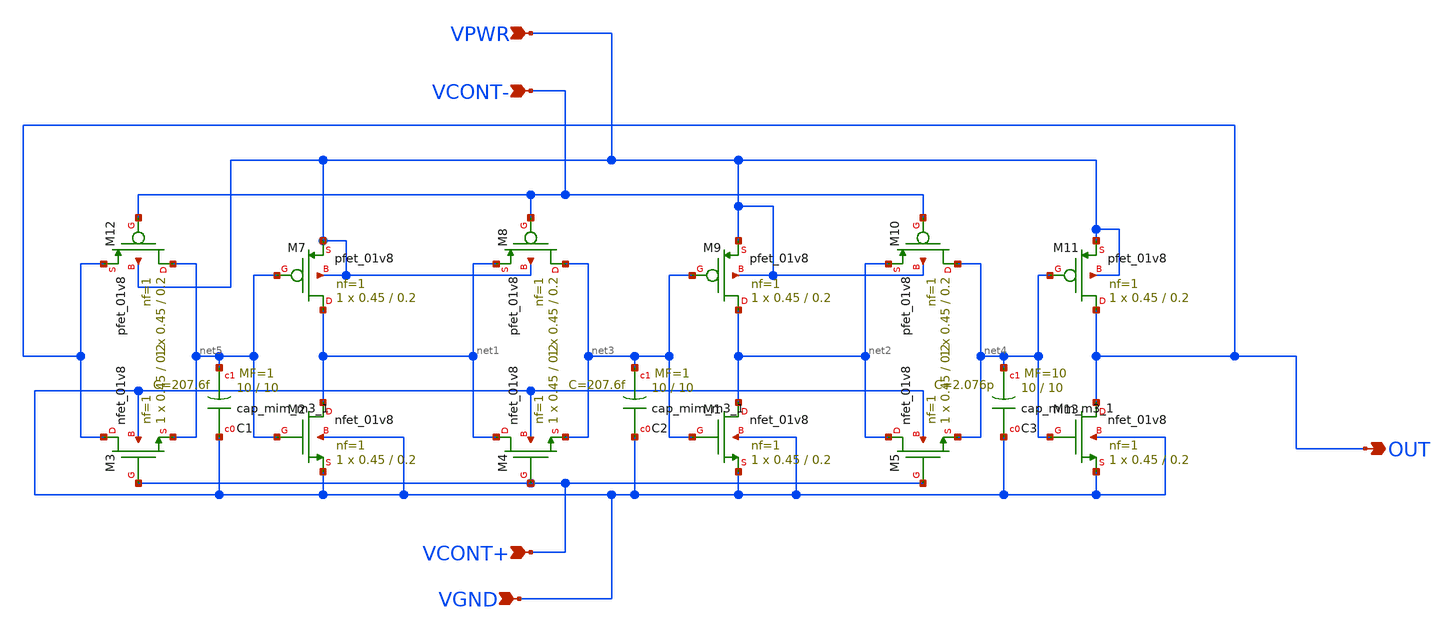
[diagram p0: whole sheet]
** sch_path: xschem_sch/ring-oscillator_with_tg.sch
**.subckt ring-oscillator_with_tg VPWR OUT VGND VCONT+ VCONT-
*.ipin VPWR
*.opin OUT
*.ipin VGND
*.ipin VCONT+
*.ipin VCONT-
XM7 net1 net5 VPWR VPWR sky130_fd_pr__pfet_01v8 L=0.2 W=0.45 nf=1 ad='int((nf+1)/2) * W/nf * 0.29' as='int((nf+2)/2) * W/nf * 0.29'
+ pd='2*int((nf+1)/2) * (W/nf + 0.29)' ps='2*int((nf+2)/2) * (W/nf + 0.29)' nrd='0.29 / W' nrs='0.29 / W'
+ sa=0 sb=0 sd=0 mult=1 m=1
XM8 net3 VCONT- net1 VPWR sky130_fd_pr__pfet_01v8 L=0.2 W=0.45 nf=1 ad='int((nf+1)/2) * W/nf * 0.29'
+ as='int((nf+2)/2) * W/nf * 0.29' pd='2*int((nf+1)/2) * (W/nf + 0.29)' ps='2*int((nf+2)/2) * (W/nf + 0.29)'
+ nrd='0.29 / W' nrs='0.29 / W' sa=0 sb=0 sd=0 mult=1 m=1
XM9 net2 net3 VPWR VPWR sky130_fd_pr__pfet_01v8 L=0.2 W=0.45 nf=1 ad='int((nf+1)/2) * W/nf * 0.29' as='int((nf+2)/2) * W/nf * 0.29'
+ pd='2*int((nf+1)/2) * (W/nf + 0.29)' ps='2*int((nf+2)/2) * (W/nf + 0.29)' nrd='0.29 / W' nrs='0.29 / W'
+ sa=0 sb=0 sd=0 mult=1 m=1
XM11 OUT net4 VPWR VPWR sky130_fd_pr__pfet_01v8 L=0.2 W=0.45 nf=1 ad='int((nf+1)/2) * W/nf * 0.29' as='int((nf+2)/2) * W/nf * 0.29'
+ pd='2*int((nf+1)/2) * (W/nf + 0.29)' ps='2*int((nf+2)/2) * (W/nf + 0.29)' nrd='0.29 / W' nrs='0.29 / W'
+ sa=0 sb=0 sd=0 mult=1 m=1
XM10 net4 VCONT- net2 VPWR sky130_fd_pr__pfet_01v8 L=0.2 W=0.45 nf=1 ad='int((nf+1)/2) * W/nf * 0.29'
+ as='int((nf+2)/2) * W/nf * 0.29' pd='2*int((nf+1)/2) * (W/nf + 0.29)' ps='2*int((nf+2)/2) * (W/nf + 0.29)'
+ nrd='0.29 / W' nrs='0.29 / W' sa=0 sb=0 sd=0 mult=1 m=1
XM12 net5 VCONT- OUT VPWR sky130_fd_pr__pfet_01v8 L=0.2 W=0.45 nf=1 ad='int((nf+1)/2) * W/nf * 0.29'
+ as='int((nf+2)/2) * W/nf * 0.29' pd='2*int((nf+1)/2) * (W/nf + 0.29)' ps='2*int((nf+2)/2) * (W/nf + 0.29)'
+ nrd='0.29 / W' nrs='0.29 / W' sa=0 sb=0 sd=0 mult=1 m=1
XC1 VGND net5 sky130_fd_pr__cap_mim_m3_1 W=10 L=10 MF=1 m=1
XC2 VGND net3 sky130_fd_pr__cap_mim_m3_1 W=10 L=10 MF=1 m=1
XC3 VGND net4 sky130_fd_pr__cap_mim_m3_1 W=10 L=10 MF=10 m=10
XM13 OUT net4 VGND VGND sky130_fd_pr__nfet_01v8 L=0.2 W=0.45 nf=1 ad='int((nf+1)/2) * W/nf * 0.29' as='int((nf+2)/2) * W/nf * 0.29'
+ pd='2*int((nf+1)/2) * (W/nf + 0.29)' ps='2*int((nf+2)/2) * (W/nf + 0.29)' nrd='0.29 / W' nrs='0.29 / W'
+ sa=0 sb=0 sd=0 mult=1 m=1
XM1 net2 net3 VGND VGND sky130_fd_pr__nfet_01v8 L=0.2 W=0.45 nf=1 ad='int((nf+1)/2) * W/nf * 0.29' as='int((nf+2)/2) * W/nf * 0.29'
+ pd='2*int((nf+1)/2) * (W/nf + 0.29)' ps='2*int((nf+2)/2) * (W/nf + 0.29)' nrd='0.29 / W' nrs='0.29 / W'
+ sa=0 sb=0 sd=0 mult=1 m=1
XM2 net1 net5 VGND VGND sky130_fd_pr__nfet_01v8 L=0.2 W=0.45 nf=1 ad='int((nf+1)/2) * W/nf * 0.29' as='int((nf+2)/2) * W/nf * 0.29'
+ pd='2*int((nf+1)/2) * (W/nf + 0.29)' ps='2*int((nf+2)/2) * (W/nf + 0.29)' nrd='0.29 / W' nrs='0.29 / W'
+ sa=0 sb=0 sd=0 mult=1 m=1
XM3 OUT VCONT+ net5 VGND sky130_fd_pr__nfet_01v8 L=0.2 W=0.45 nf=1 ad='int((nf+1)/2) * W/nf * 0.29' as='int((nf+2)/2) * W/nf * 0.29'
+ pd='2*int((nf+1)/2) * (W/nf + 0.29)' ps='2*int((nf+2)/2) * (W/nf + 0.29)' nrd='0.29 / W' nrs='0.29 / W'
+ sa=0 sb=0 sd=0 mult=1 m=1
XM4 net1 VCONT+ net3 VGND sky130_fd_pr__nfet_01v8 L=0.2 W=0.45 nf=1 ad='int((nf+1)/2) * W/nf * 0.29'
+ as='int((nf+2)/2) * W/nf * 0.29' pd='2*int((nf+1)/2) * (W/nf + 0.29)' ps='2*int((nf+2)/2) * (W/nf + 0.29)'
+ nrd='0.29 / W' nrs='0.29 / W' sa=0 sb=0 sd=0 mult=1 m=1
XM5 net2 VCONT+ net4 VGND sky130_fd_pr__nfet_01v8 L=0.2 W=0.45 nf=1 ad='int((nf+1)/2) * W/nf * 0.29'
+ as='int((nf+2)/2) * W/nf * 0.29' pd='2*int((nf+1)/2) * (W/nf + 0.29)' ps='2*int((nf+2)/2) * (W/nf + 0.29)'
+ nrd='0.29 / W' nrs='0.29 / W' sa=0 sb=0 sd=0 mult=1 m=1
**.ends
.end
